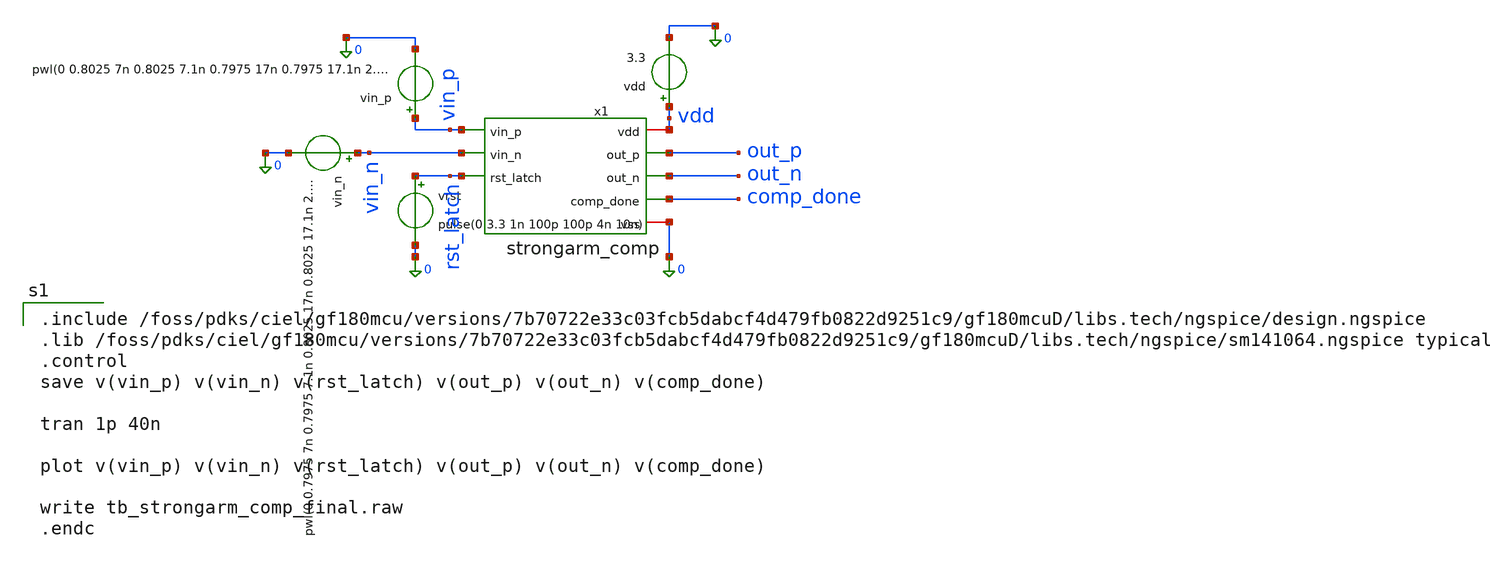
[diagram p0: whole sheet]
** sch_path: xschem/sar_adc/testbench/tb_strongarm_comp_final.sch
**.subckt tb_strongarm_comp_final
vdd vdd 0 3.3
vin_p vin_p 0 pwl(0 0.8025 7n 0.8025 7.1n 0.7975 17n 0.7975 17.1n 2.5025 27n 2.5025 27.1n 2.4975 40n
+ 2.4975)
vin_n vin_n 0 pwl(0 0.7975 7n 0.7975 7.1n 0.8025 17n 0.8025 17.1n 2.4975 27n 2.4975 27.1n 2.5025 40n
+ 2.5025)
vrst rst_latch 0 pulse(0 3.3 1n 100p 100p 4n 10n)
x1 vdd vin_p out_p vin_n out_n comp_done rst_latch 0 strongarm_comp
**** begin user architecture code

.include /foss/pdks/ciel/gf180mcu/versions/7b70722e33c03fcb5dabcf4d479fb0822d9251c9/gf180mcuD/libs.tech/ngspice/design.ngspice
.lib /foss/pdks/ciel/gf180mcu/versions/7b70722e33c03fcb5dabcf4d479fb0822d9251c9/gf180mcuD/libs.tech/ngspice/sm141064.ngspice typical
.control
save v(vin_p) v(vin_n) v(rst_latch) v(out_p) v(out_n) v(comp_done)

tran 1p 40n

plot v(vin_p) v(vin_n) v(rst_latch) v(out_p) v(out_n) v(comp_done)

write tb_strongarm_comp_final.raw
.endc

**** end user architecture code
**.ends
.end
